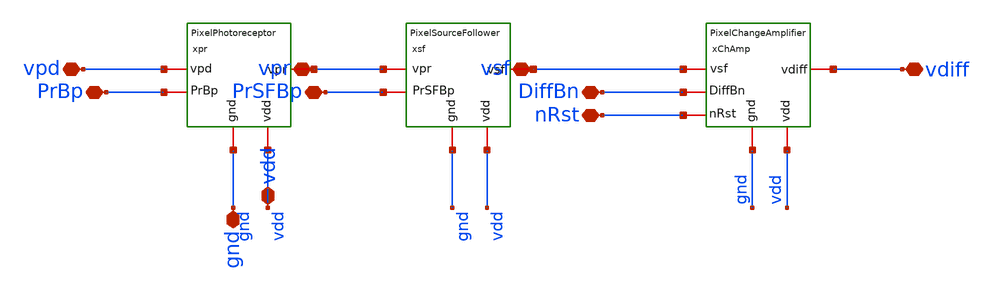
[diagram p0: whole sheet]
** sch_path: analog/xschem/PixelGainAC.sch
**.subckt PixelGainAC vpd PrBp PrSFBp nRst DiffBn vdiff vpr vsf gnd vdd
*.iopin vpd
*.iopin PrBp
*.iopin PrSFBp
*.iopin nRst
*.iopin DiffBn
*.iopin vdiff
*.iopin vpr
*.iopin vsf
*.iopin gnd
*.iopin vdd
xpr vdd PrBp gnd vpd vpr PixelPhotoreceptor
xsf vdd PrSFBp gnd vpr vsf PixelSourceFollower
xChAmp vdd DiffBn gnd vsf vdiff nRst PixelChangeAmplifier
**.ends

* expanding   symbol:  PixelPhotoreceptor.sym # of pins=5
** sym_path: analog/xschem/PixelPhotoreceptor.sym
** sch_path: analog/xschem/PixelPhotoreceptor.sch
.subckt PixelPhotoreceptor vdd PrBp gnd vpd vpr
*.iopin PrBp
*.iopin vdd
*.iopin vpd
*.iopin gnd
*.iopin vpr
XMpd vdd vpr vpd gnd sky130_fd_pr__nfet_01v8 L=0.3 W=0.5 nf=1 ad='int((1 + 1)/2) * 0.5 / 1 * 0.29' as='int((1 + 2)/2) * 0.5 / 1 * 0.29'
+ pd='2*int((1 + 1)/2) * (0.5 / 1 + 0.29)' ps='2*int((1 + 2)/2) * (0.5 / 1 + 0.29)' nrd='0.29 / 0.5 ' nrs='0.29 / 0.5 '
+ sa=0 sb=0 sd=0 mult=1 m=1
XMpr_amp vpr vpd gnd gnd sky130_fd_pr__nfet_01v8 L=0.3 W=0.5 nf=1 ad='int((1 + 1)/2) * 0.5 / 1 * 0.29'
+ as='int((1 + 2)/2) * 0.5 / 1 * 0.29' pd='2*int((1 + 1)/2) * (0.5 / 1 + 0.29)' ps='2*int((1 + 2)/2) * (0.5 / 1 + 0.29)'
+ nrd='0.29 / 0.5 ' nrs='0.29 / 0.5 ' sa=0 sb=0 sd=0 mult=1 m=1
XMprBias vpr PrBp vdd vdd sky130_fd_pr__pfet_01v8_hvt L=0.3 W=1 nf=1 ad='int((1 + 1)/2) * 1 / 1 * 0.29'
+ as='int((1 + 2)/2) * 1 / 1 * 0.29' pd='2*int((1 + 1)/2) * (1 / 1 + 0.29)' ps='2*int((1 + 2)/2) * (1 / 1 + 0.29)'
+ nrd='0.29 / 1 ' nrs='0.29 / 1 ' sa=0 sb=0 sd=0 mult=1 m=1
.ends


* expanding   symbol:  PixelSourceFollower.sym # of pins=5
** sym_path: analog/xschem/PixelSourceFollower.sym
** sch_path: analog/xschem/PixelSourceFollower.sch
.subckt PixelSourceFollower vdd PrSFBp gnd vpr vsf
*.iopin gnd
*.iopin PrSFBp
*.iopin vpr
*.iopin vsf
*.iopin vdd
XMsfBias vsf PrSFBp vdd vdd sky130_fd_pr__pfet_01v8 L=4 W=1 nf=1 ad='int((1 + 1)/2) * 1 / 1 * 0.29' as='int((1 + 2)/2) * 1 / 1 * 0.29'
+ pd='2*int((1 + 1)/2) * (1 / 1 + 0.29)' ps='2*int((1 + 2)/2) * (1 / 1 + 0.29)' nrd='0.29 / 1 ' nrs='0.29 / 1 '
+ sa=0 sb=0 sd=0 mult=1 m=1
XMsf1 gnd vpr vsf vdd sky130_fd_pr__pfet_01v8 L=1 W=2 nf=1 ad='int((1 + 1)/2) * 2 / 1 * 0.29' as='int((1 + 2)/2) * 2 / 1 * 0.29'
+ pd='2*int((1 + 1)/2) * (2 / 1 + 0.29)' ps='2*int((1 + 2)/2) * (2 / 1 + 0.29)' nrd='0.29 / 2 ' nrs='0.29 / 2 '
+ sa=0 sb=0 sd=0 mult=1 m=1
.ends


* expanding   symbol:  PixelChangeAmplifier.sym # of pins=6
** sym_path: analog/xschem/PixelChangeAmplifier.sym
** sch_path: analog/xschem/PixelChangeAmplifier.sch
.subckt PixelChangeAmplifier vdd DiffBn gnd vsf vdiff nRst
*.iopin DiffBn
*.iopin vsf
*.iopin vdd
*.iopin gnd
*.iopin vdiff
*.iopin nRst
XC1 vsf vd sky130_fd_pr__cap_mim_m3_1 W=1 L=1 MF=40 m=40
XC2 vd vdiff sky130_fd_pr__cap_mim_m3_1 W=1 L=1 MF=2 m=2
XMchAmpBias vdiff DiffBn gnd gnd sky130_fd_pr__nfet_01v8 L=2 W=2 nf=1 ad='int((1 + 1)/2) * 2 / 1 * 0.29'
+ as='int((1 + 2)/2) * 2 / 1 * 0.29' pd='2*int((1 + 1)/2) * (2 / 1 + 0.29)' ps='2*int((1 + 2)/2) * (2 / 1 + 0.29)'
+ nrd='0.29 / 2 ' nrs='0.29 / 2 ' sa=0 sb=0 sd=0 mult=1 m=1
XMrst vdiff nRst vd vdd sky130_fd_pr__pfet_01v8_hvt L=0.3 W=1 nf=1 ad='int((1 + 1)/2) * 1 / 1 * 0.29'
+ as='int((1 + 2)/2) * 1 / 1 * 0.29' pd='2*int((1 + 1)/2) * (1 / 1 + 0.29)' ps='2*int((1 + 2)/2) * (1 / 1 + 0.29)'
+ nrd='0.29 / 1 ' nrs='0.29 / 1 ' sa=0 sb=0 sd=0 mult=1 m=1
XMchAmp vdiff vd vdd vdd sky130_fd_pr__pfet_01v8_hvt L=2 W=2 nf=1 ad='int((1 + 1)/2) * 2 / 1 * 0.29'
+ as='int((1 + 2)/2) * 2 / 1 * 0.29' pd='2*int((1 + 1)/2) * (2 / 1 + 0.29)' ps='2*int((1 + 2)/2) * (2 / 1 + 0.29)'
+ nrd='0.29 / 2 ' nrs='0.29 / 2 ' sa=0 sb=0 sd=0 mult=1 m=1
.ends

.end
